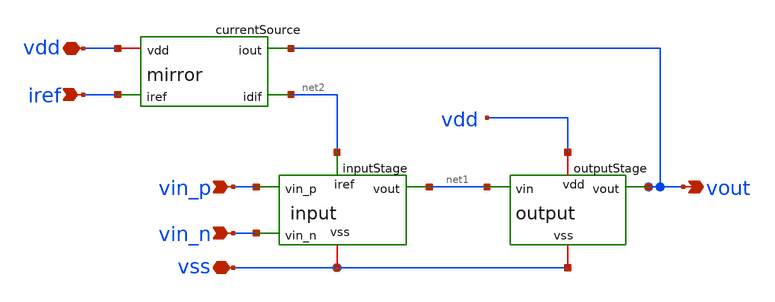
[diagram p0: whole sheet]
** sch_path: track_analogico/opamp_ramiro/schematic_hier.sch
**.subckt schematic_hier vdd vss vin_n iref vout vin_p
*.iopin vdd
*.iopin vss
*.ipin vin_n
*.ipin iref
*.opin vout
*.ipin vin_p
inputStage net2 vin_p vin_n net1 vss input
currentSource vdd net2 vout iref mirror
outputStage vout vdd net1 vss output
**.ends
.end
